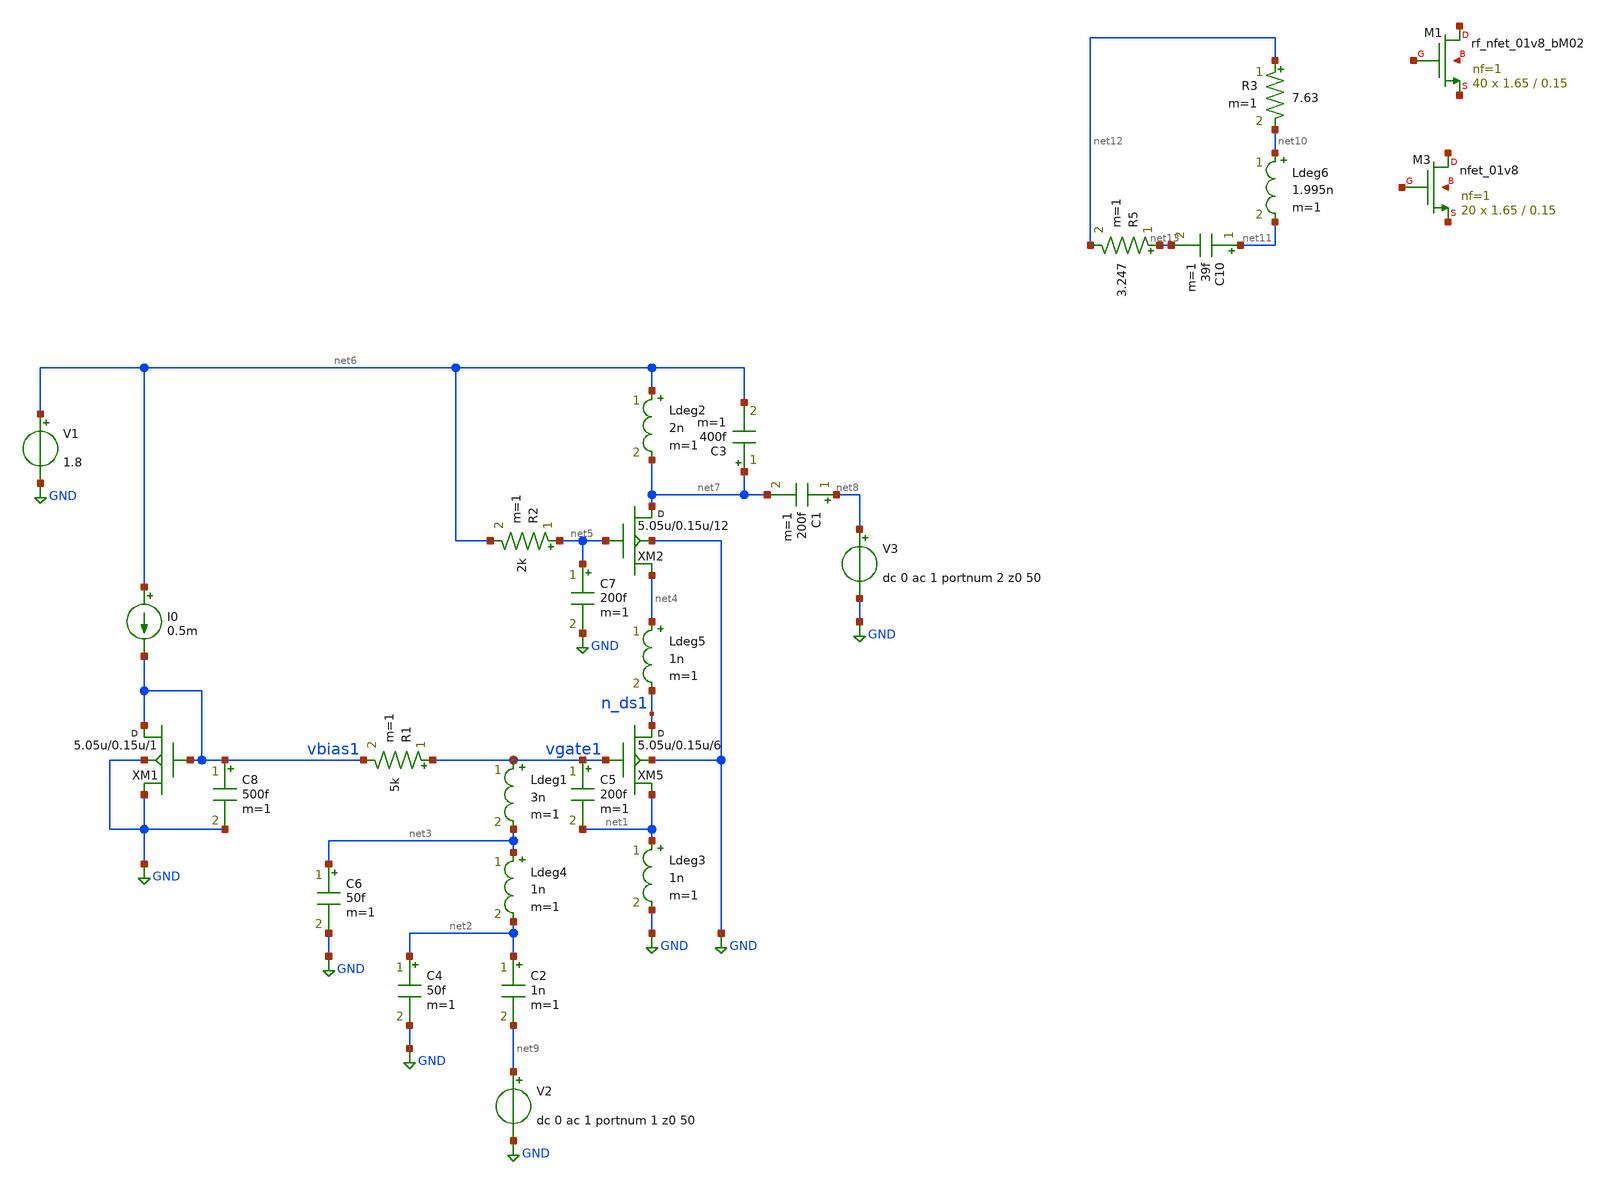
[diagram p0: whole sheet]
** sch_path: xschem/zptest_1.sch
**.subckt zptest_1
V1 net6 GND 1.8
C1 net8 net7 200f m=1
V2 net9 GND dc 0 ac 1 portnum 1 z0 50
V3 net8 GND dc 0 ac 1 portnum 2 z0 50
Ldeg3 net1 GND 1n m=1
C2 net2 net9 1n m=1
R1 vgate1 vbias1 5k m=1
XM3 net14 net15 net16 net17 sky130_fd_pr__nfet_01v8 L=0.15 W=1.65 nf=1 ad='int((nf+1)/2) * W/nf * 0.29'
+ as='int((nf+2)/2) * W/nf * 0.29' pd='2*int((nf+1)/2) * (W/nf + 0.29)' ps='2*int((nf+2)/2) * (W/nf + 0.29)'
+ nrd='0.29 / W' nrs='0.29 / W' sa=0 sb=0 sd=0 mult=20 m=20
Ldeg5 net4 n_ds1 1n m=1
C4 net2 GND 50f m=1
Ldeg1 vgate1 net3 3n m=1
C5 vgate1 net1 200f m=1
Ldeg4 net3 net2 1n m=1
C6 net3 GND 50f m=1
Ldeg6 net10 net11 1.995n m=1
R2 net5 net6 2k m=1
C7 net5 GND 200f m=1
C3 net7 net6 400f m=1
I0 net6 vbias1 0.5m
C8 vbias1 GND 500f m=1
R3 net12 net10 7.63 m=1
C10 net11 net13 39f m=1
R5 net13 net12 3.247 m=1
Ldeg2 net6 net7 2n m=1
XM5 n_ds1 vgate1 net1 GND sky130_fd_pr__rf_nfet_01v8_bM04W5p00L0p15_ext w=5.05u l=0.15u m=6
XM1 vbias1 vbias1 GND GND sky130_fd_pr__rf_nfet_01v8_bM04W5p00L0p15_ext w=5.05u l=0.15u m=1
XM1 net18 net19 net20 net21 sky130_fd_pr__rf_nfet_01v8_bM02 L=0.15 W=1.65 nf=1 ad='int((nf+1)/2) * W/nf * 0.29'
+ as='int((nf+2)/2) * W/nf * 0.29' pd='2*int((nf+1)/2) * (W/nf + 0.29)' ps='2*int((nf+2)/2) * (W/nf + 0.29)'
+ nrd='0.29 / W' nrs='0.29 / W' sa=0 sb=0 sd=0 mult=40 m=40
XM2 net7 net5 net4 GND sky130_fd_pr__rf_nfet_01v8_bM04W5p00L0p15_ext w=5.05u l=0.15u m=12
**** begin user architecture code
.lib $::SKYWATER_MODELS/sky130.lib.spice tt
* .include $::PDKPATH/libs.ref/sky130_fd_sc_hvl/spice/sky130_fd_sc_hvl.spice



.subckt sky130_fd_pr__rf_nfet_01v8_bM04W5p00L0p15_ext DRAIN GATE SOURCE SUBSTRATE
X0 DRAIN GATE SOURCE SUBSTRATE sky130_fd_pr__nfet_01v8 ad=2.828e+12p pd=2.132e+07u as=4.242e+12p
+ ps=3.198e+07u w=5.05e+06u l=150000u
X1 SOURCE SUBSTRATE SUBSTRATE SUBSTRATE sky130_fd_pr__nfet_01v8 ad=0p pd=0u as=3.03e+12p
+ ps=2.14e+07u w=5.05e+06u l=150000u
X2 SOURCE GATE DRAIN SUBSTRATE sky130_fd_pr__nfet_01v8 ad=0p pd=0u as=0p ps=0u w=5.05e+06u l=150000u
X3 DRAIN GATE SOURCE SUBSTRATE sky130_fd_pr__nfet_01v8 ad=0p pd=0u as=0p ps=0u w=5.05e+06u l=150000u
X4 SUBSTRATE SUBSTRATE SOURCE SUBSTRATE sky130_fd_pr__nfet_01v8 ad=0p pd=0u as=0p ps=0u w=5.05e+06u
+ l=150000u
X5 SOURCE GATE DRAIN SUBSTRATE sky130_fd_pr__nfet_01v8 ad=0p pd=0u as=0p ps=0u w=5.05e+06u l=150000u
.ends
.sp dec 1000 0.01e9 20e9 0
* .ac dec 1000 0.01e9 100e9
.control
run
display
let z11=50*(1+s_1_1)/(1-s_1_1)
let z22=50*(1+s_2_2)/(1-s_2_2)
plot real(z11) real(z22)
plot imag(z11) imag(z22)
plot db(S_1_1) db(S_2_2) db(S_2_1)
.endc


**** end user architecture code
**.ends
.GLOBAL GND
.end
